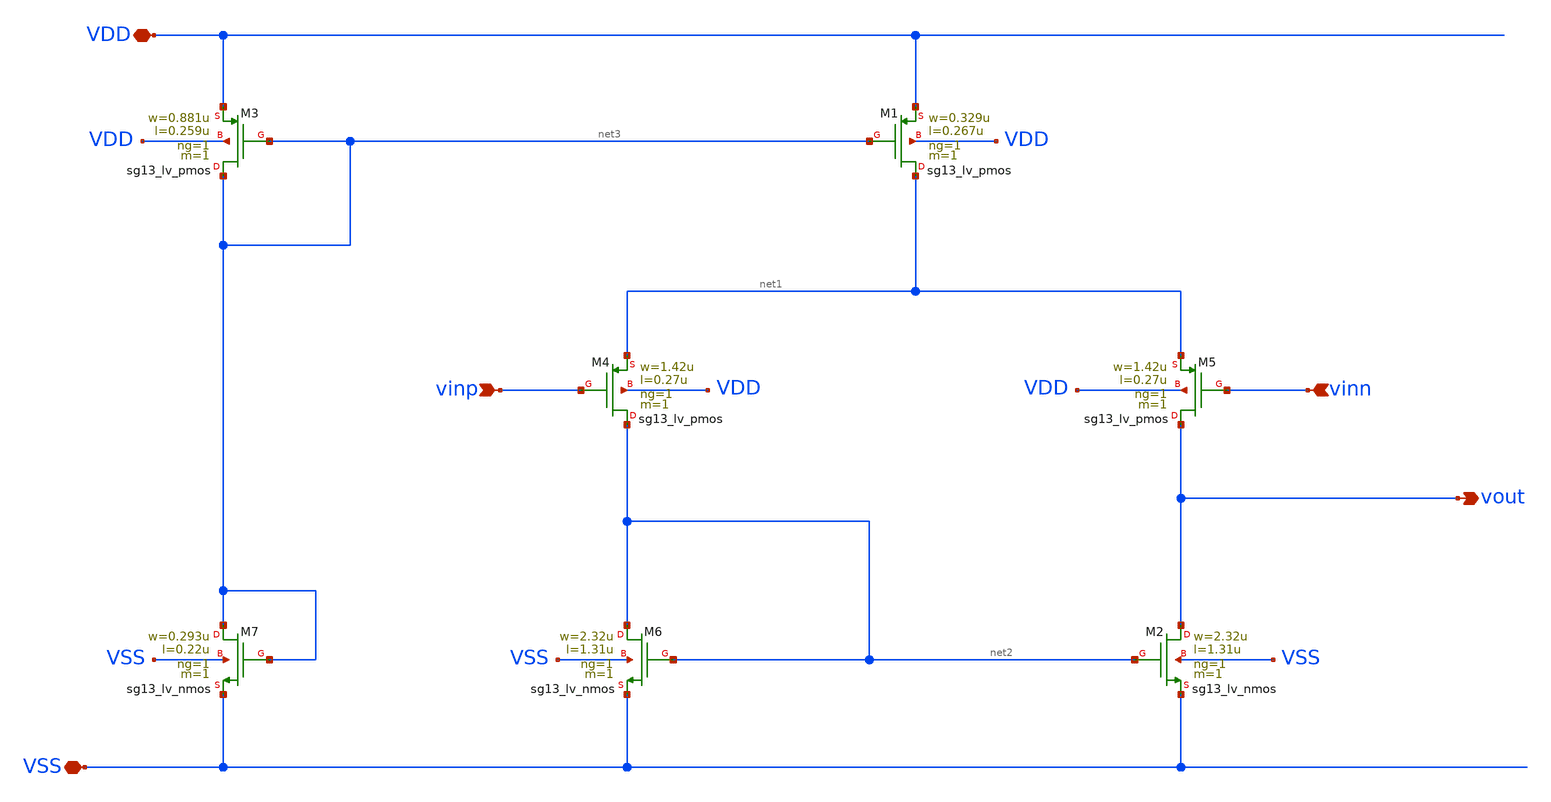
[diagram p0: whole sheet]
** sch_path: analog-db/drawings/shared/amp-single-ended-5t-pmos-input.sch
* Copyright 2026 MacAnalog Research Group
**.subckt amp-single-ended-5t-pmos-input vinp vinn VSS VDD vout
*.ipin vinp
*.ipin vinn
*.iopin VSS
*.iopin VDD
*.opin vout
XM1 net1 net3 VDD VDD sg13_lv_pmos w=0.329u l=0.267u ng=1 m=1 mm_ok=1
XM2 vout net2 VSS VSS sg13_lv_nmos w=2.32u l=1.31u ng=1 m=1 mm_ok=1
XM3 net3 net3 VDD VDD sg13_lv_pmos w=0.881u l=0.259u ng=1 m=1 mm_ok=1
XM4 net2 vinp net1 VDD sg13_lv_pmos w=1.42u l=0.27u ng=1 m=1 mm_ok=1
XM5 vout vinn net1 VDD sg13_lv_pmos w=1.42u l=0.27u ng=1 m=1 mm_ok=1
XM6 net2 net2 VSS VSS sg13_lv_nmos w=2.32u l=1.31u ng=1 m=1 mm_ok=1
XM7 net3 net3 VSS VSS sg13_lv_nmos w=0.293u l=0.22u ng=1 m=1 mm_ok=1
**.ends
.end
